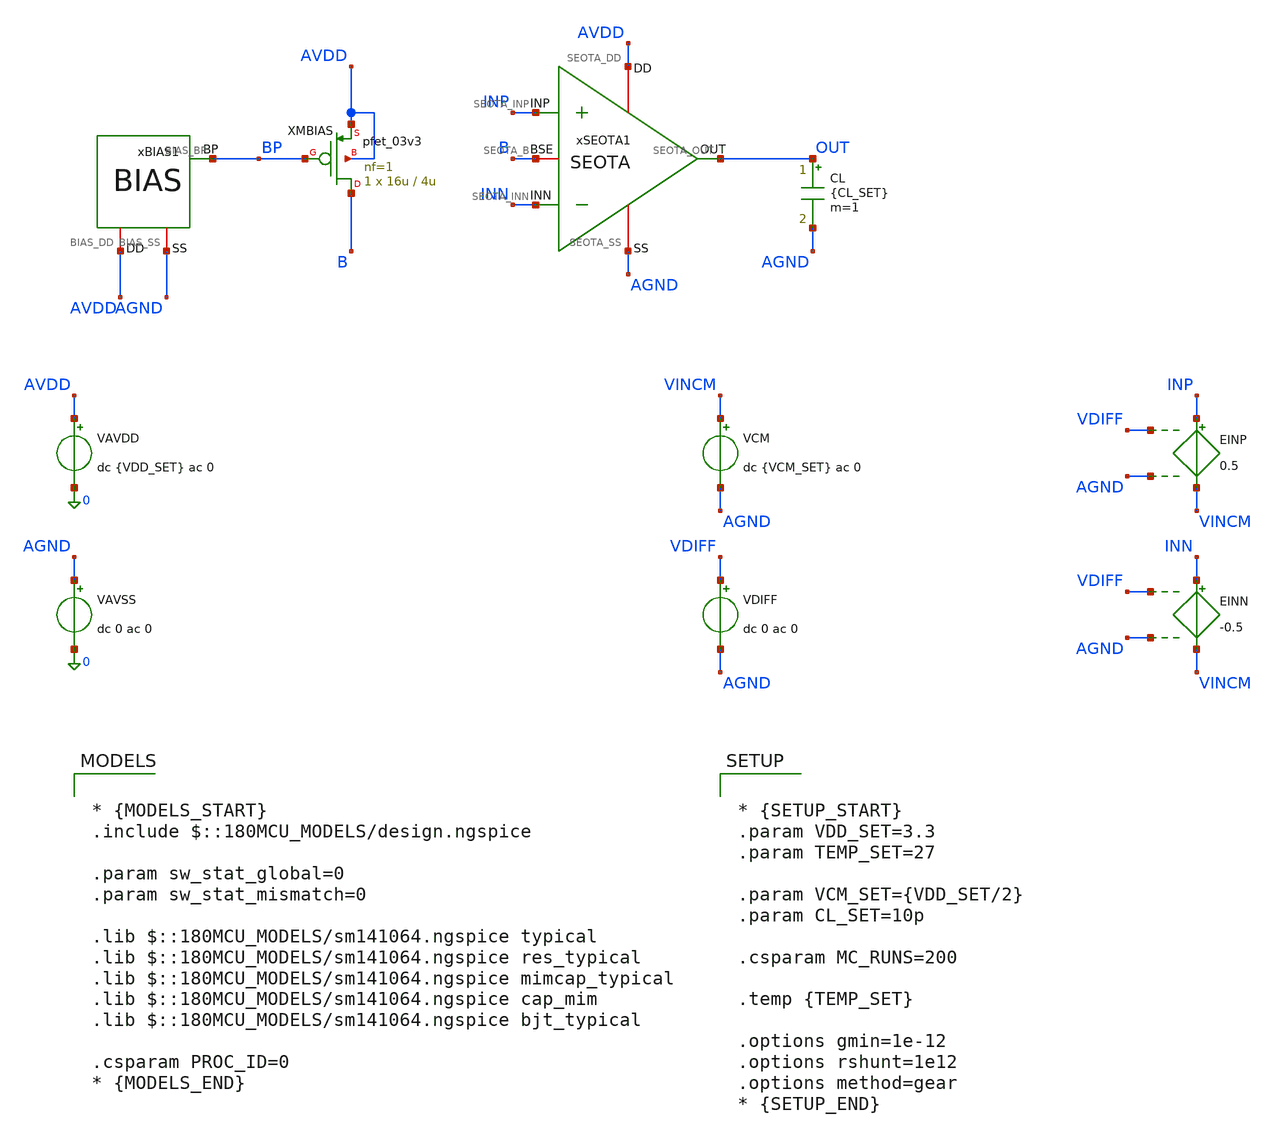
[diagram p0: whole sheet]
** sch_path: Design_Files/IC Design/Testbench/ANALOG_BLOCKS/SEOTA/Open_Loop/SEOTA_TB_OL_PVT_NOM.sch
**.subckt SEOTA_TB_OL_PVT_NOM
VAVDD AVDD 0 dc {VDD_SET} ac 0
.save i(vavdd)
CL OUT AGND {CL_SET} m=1
VCM VINCM AGND dc {VCM_SET} ac 0
VDIFF VDIFF AGND dc 0 ac 0
xSEOTA1 AVDD AGND INP INN OUT B SEOTA
VAVSS AGND 0 dc 0 ac 0
EINN INN VINCM VDIFF AGND -0.5
EINP INP VINCM VDIFF AGND 0.5
xBIAS1 AVDD AGND BP BIAS
XMBIAS B BP AVDD AVDD pfet_03v3 L=4u W=16u nf=1 ad='int((nf+1)/2) * W/nf * 0.18u' as='int((nf+2)/2) * W/nf * 0.18u'
+ pd='2*int((nf+1)/2) * (W/nf + 0.18u)' ps='2*int((nf+2)/2) * (W/nf + 0.18u)' nrd='0.18u / W' nrs='0.18u / W'
+ sa=0 sb=0 sd=0 m=1
**** begin user architecture code

* {MODELS_START}
.include $::180MCU_MODELS/design.ngspice

.param sw_stat_global=0
.param sw_stat_mismatch=0

.lib $::180MCU_MODELS/sm141064.ngspice typical
.lib $::180MCU_MODELS/sm141064.ngspice res_typical
.lib $::180MCU_MODELS/sm141064.ngspice mimcap_typical
.lib $::180MCU_MODELS/sm141064.ngspice cap_mim
.lib $::180MCU_MODELS/sm141064.ngspice bjt_typical

.csparam PROC_ID=0
* {MODELS_END}



* {SETUP_START}
.param VDD_SET=3.3
.param TEMP_SET=27

.param VCM_SET={VDD_SET/2}
.param CL_SET=10p

.csparam MC_RUNS=200

.temp {TEMP_SET}

.options gmin=1e-12
.options rshunt=1e12
.options method=gear
* {SETUP_END}




* {MEAS_START}

.control

destroy all

set noaskquit
set wr_singlescale
unset wr_vecnames

option klu
option numdgt=15
option method=gear
option maxord=2
option plotwinsize=0


if $&PROC_ID = 0
set proc=NOM
else
if $&PROC_ID = 1
set proc=FF
else
if $&PROC_ID = 2
set proc=SS
else
if $&PROC_ID = 3
set proc=FS
else
set proc=SF
end
end
end
end


shell mkdir -p /foss/designs/ECG_Acquisition_IC/Measurement_Results/IC_Simulation/ANALOG_BLOCKS/SEOTA/{$proc}.Result_txt
shell rm -f /foss/designs/ECG_Acquisition_IC/Measurement_Results/IC_Simulation/ANALOG_BLOCKS/SEOTA/{$proc}.Result_txt/{$proc}.ol_*.txt


foreach vddval 3.3 3.0 3.6
foreach tval 27 -40 125


if $vddval = 3.3

if $tval = 27
set case=nom
else
if $tval = -40
set case=tl
else
set case=th
end
end

else

if $vddval = 3.0

if $tval = 27
set case=vl
else
if $tval = -40
set case=vltl
else
set case=vlth
end
end

else

if $tval = 27
set case=vh
else
if $tval = -40
set case=vhtl
else
set case=vhth
end
end

end
end


alterparam VDD_SET=$vddval
alterparam TEMP_SET=$tval

reset

option klu

save all
save @m.xmbias.m0[id]


* OP

op

let vdd=v(AVDD)-v(AGND)
let vinp=v(INP)-v(AGND)
let vinn=v(INN)-v(AGND)
let vout=v(OUT)-v(AGND)

let idd_total=abs(vavdd#branch)
let ibias=abs(@m.xmbias.m0[id])

wrdata /foss/designs/ECG_Acquisition_IC/Measurement_Results/IC_Simulation/ANALOG_BLOCKS/SEOTA/{$proc}.Result_txt/{$proc}.ol_{$case}_op.txt
+ vdd vinp vinn vout v(B) idd_total ibias


* DIFFERENTIAL AC

alter @VCM[ACMAG]=0
alter @VDIFF[ACMAG]=1
alter @VDIFF[ACPHASE]=0
alter @VAVDD[ACMAG]=0
alter @VAVSS[ACMAG]=0

ac dec 200 0.01 1G

let vin_diff=v(INP)-v(INN)
let vout=v(OUT)-v(AGND)

let vin_diff_real=real(vin_diff)
let vin_diff_imag=imag(vin_diff)

let vout_real=real(vout)
let vout_imag=imag(vout)

setscale frequency

wrdata /foss/designs/ECG_Acquisition_IC/Measurement_Results/IC_Simulation/ANALOG_BLOCKS/SEOTA/{$proc}.Result_txt/{$proc}.ol_{$case}_diff_ac.txt
+ vin_diff_real vin_diff_imag vout_real vout_imag


* COMMON-MODE AC

alter @VCM[ACMAG]=1
alter @VCM[ACPHASE]=0
alter @VDIFF[ACMAG]=0
alter @VAVDD[ACMAG]=0
alter @VAVSS[ACMAG]=0

ac dec 200 0.01 1G

let vin_cm=0.5*(v(INP)+v(INN))-v(AGND)
let vout=v(OUT)-v(AGND)

let vin_cm_real=real(vin_cm)
let vin_cm_imag=imag(vin_cm)

let vout_real=real(vout)
let vout_imag=imag(vout)

setscale frequency

wrdata /foss/designs/ECG_Acquisition_IC/Measurement_Results/IC_Simulation/ANALOG_BLOCKS/SEOTA/{$proc}.Result_txt/{$proc}.ol_{$case}_cm_ac.txt
+ vin_cm_real vin_cm_imag vout_real vout_imag


* PSRRP

alter @VCM[ACMAG]=0
alter @VDIFF[ACMAG]=0
alter @VAVDD[ACMAG]=1
alter @VAVDD[ACPHASE]=0
alter @VAVSS[ACMAG]=0

ac dec 200 0.01 1G

let vsup=v(AVDD)-v(AGND)
let vout=v(OUT)-v(AGND)

let vsup_real=real(vsup)
let vsup_imag=imag(vsup)

let vout_real=real(vout)
let vout_imag=imag(vout)

setscale frequency

wrdata /foss/designs/ECG_Acquisition_IC/Measurement_Results/IC_Simulation/ANALOG_BLOCKS/SEOTA/{$proc}.Result_txt/{$proc}.ol_{$case}_psrrp_ac.txt
+ vsup_real vsup_imag vout_real vout_imag


* PSRRN

alter @VCM[ACMAG]=0
alter @VDIFF[ACMAG]=0
alter @VAVDD[ACMAG]=0
alter @VAVSS[ACMAG]=1
alter @VAVSS[ACPHASE]=0

ac dec 200 0.01 1G

let vagnd=v(AGND)
let vout=v(OUT)-v(AGND)

let vagnd_real=real(vagnd)
let vagnd_imag=imag(vagnd)

let vout_real=real(vout)
let vout_imag=imag(vout)

setscale frequency

wrdata /foss/designs/ECG_Acquisition_IC/Measurement_Results/IC_Simulation/ANALOG_BLOCKS/SEOTA/{$proc}.Result_txt/{$proc}.ol_{$case}_psrrn_ac.txt
+ vagnd_real vagnd_imag vout_real vout_imag


* VTC

alter @VCM[ACMAG]=0
alter @VDIFF[ACMAG]=0
alter @VAVDD[ACMAG]=0
alter @VAVSS[ACMAG]=0

dc VDIFF -20m 20m 1u

let vin_cm=0.5*(v(INP)+v(INN))-v(AGND)
let vin_diff=v(INP)-v(INN)
let vout=v(OUT)-v(AGND)

let idd_total=abs(vavdd#branch)

setscale vin_diff

wrdata /foss/designs/ECG_Acquisition_IC/Measurement_Results/IC_Simulation/ANALOG_BLOCKS/SEOTA/{$proc}.Result_txt/{$proc}.ol_{$case}_vtc.txt
+ vin_cm v(INP) v(INN) vout idd_total


* NOISE

option sparse

alter @VCM[ACMAG]=0
alter @VDIFF[ACMAG]=1
alter @VDIFF[ACPHASE]=0
alter @VAVDD[ACMAG]=0
alter @VAVSS[ACMAG]=0

noise v(OUT) VDIFF dec 100 0.01 1k

setplot previous
setscale frequency

wrdata /foss/designs/ECG_Acquisition_IC/Measurement_Results/IC_Simulation/ANALOG_BLOCKS/SEOTA/{$proc}.Result_txt/{$proc}.ol_{$case}_noise.txt
+ onoise_spectrum inoise_spectrum


destroy all

end
end


quit

.endc
* {MEAS_END}


**** end user architecture code
**.ends
.end
